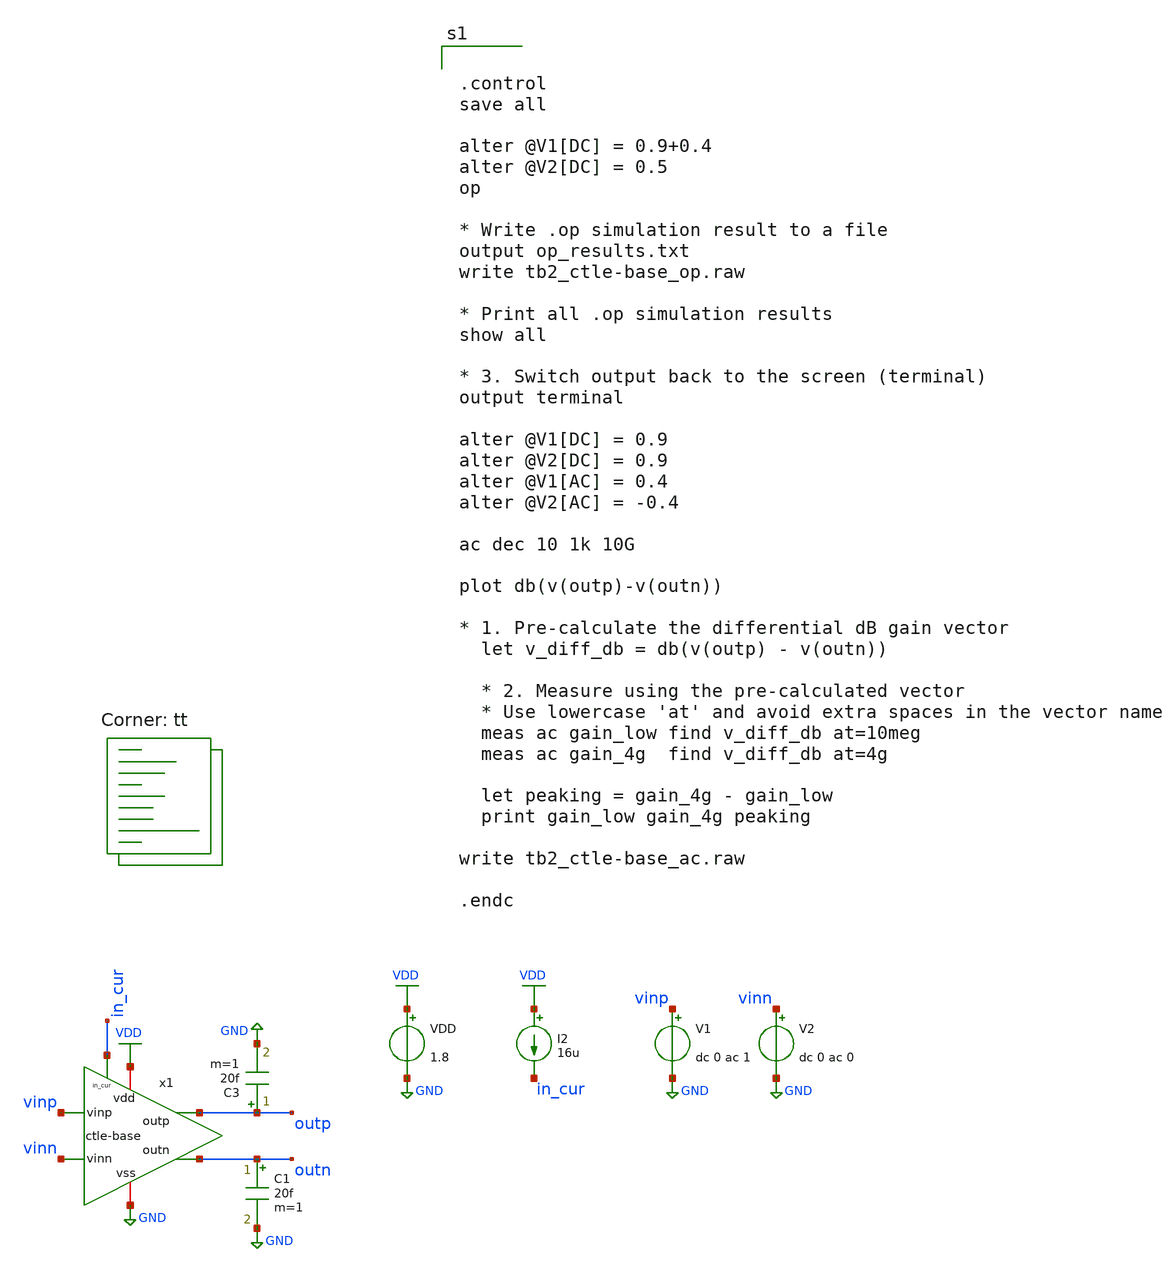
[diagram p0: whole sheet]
** sch_path: CTLE/tb2_ctle-base.sch
**.subckt tb2_ctle-base
x1 VDD GND outp outn vinn vinp in_cur ctle-base
VDD VDD GND 1.8
V1 vinp GND dc 0 ac 1
V2 vinn GND dc 0 ac 0
I2 VDD in_cur 16u
C3 outp GND 20f m=1
C1 outn GND 20f m=1
**** begin user architecture code
.lib $::SKYWATER_MODELS/sky130.lib.spice tt


.control
save all

alter @V1[DC] = 0.9+0.4
alter @V2[DC] = 0.5
op

* Write .op simulation result to a file
output op_results.txt
write tb2_ctle-base_op.raw

* Print all .op simulation results
show all

* 3. Switch output back to the screen (terminal)
output terminal

alter @V1[DC] = 0.9
alter @V2[DC] = 0.9
alter @V1[AC] = 0.4
alter @V2[AC] = -0.4

ac dec 10 1k 10G

plot db(v(outp)-v(outn))

* 1. Pre-calculate the differential dB gain vector
  let v_diff_db = db(v(outp) - v(outn))

  * 2. Measure using the pre-calculated vector
  * Use lowercase 'at' and avoid extra spaces in the vector name
  meas ac gain_low find v_diff_db at=10meg
  meas ac gain_4g  find v_diff_db at=4g

  let peaking = gain_4g - gain_low
  print gain_low gain_4g peaking

write tb2_ctle-base_ac.raw

.endc

**** end user architecture code
**.ends

* expanding   symbol:  /foss/designs/Teknofest/afe-icdec-teknofest-2026/CTLE/ctle-base.sym # of
*+ pins=7
** sym_path: CTLE/ctle-base.sym
** sch_path: CTLE/ctle-base.sch
.subckt ctle-base vdd vss outp outn vinn vinp in_cur
*.iopin vdd
*.iopin vss
*.ipin vinp
*.ipin vinn
*.opin outn
*.opin outp
*.ipin in_cur
XM1 outn vinp net1 net1 sky130_fd_pr__nfet_01v8 L=0.15 W=12.5 nf=1 ad='int((nf+1)/2) * W/nf * 0.29' as='int((nf+2)/2) * W/nf * 0.29'
+ pd='2*int((nf+1)/2) * (W/nf + 0.29)' ps='2*int((nf+2)/2) * (W/nf + 0.29)' nrd='0.29 / W' nrs='0.29 / W'
+ sa=0 sb=0 sd=0 mult=1 m=1
XM2 outp vinn net2 net2 sky130_fd_pr__nfet_01v8 L=0.15 W=12.5 nf=1 ad='int((nf+1)/2) * W/nf * 0.29' as='int((nf+2)/2) * W/nf * 0.29'
+ pd='2*int((nf+1)/2) * (W/nf + 0.29)' ps='2*int((nf+2)/2) * (W/nf + 0.29)' nrd='0.29 / W' nrs='0.29 / W'
+ sa=0 sb=0 sd=0 mult=1 m=1
XC1 net1 net2 sky130_fd_pr__cap_mim_m3_1 W=7.5 L=7.5 MF=1 m=1
XM5 in_cur in_cur vss vss sky130_fd_pr__nfet_01v8 L=0.5 W=1 nf=1 ad='int((nf+1)/2) * W/nf * 0.29' as='int((nf+2)/2) * W/nf * 0.29'
+ pd='2*int((nf+1)/2) * (W/nf + 0.29)' ps='2*int((nf+2)/2) * (W/nf + 0.29)' nrd='0.29 / W' nrs='0.29 / W'
+ sa=0 sb=0 sd=0 mult=1 m=1
XM6 net1 in_cur vss vss sky130_fd_pr__nfet_01v8 L=0.5 W=21.88 nf=1 ad='int((nf+1)/2) * W/nf * 0.29' as='int((nf+2)/2) * W/nf * 0.29'
+ pd='2*int((nf+1)/2) * (W/nf + 0.29)' ps='2*int((nf+2)/2) * (W/nf + 0.29)' nrd='0.29 / W' nrs='0.29 / W'
+ sa=0 sb=0 sd=0 mult=1 m=1
XM7 net2 in_cur vss vss sky130_fd_pr__nfet_01v8 L=0.5 W=21.88 nf=1 ad='int((nf+1)/2) * W/nf * 0.29' as='int((nf+2)/2) * W/nf * 0.29'
+ pd='2*int((nf+1)/2) * (W/nf + 0.29)' ps='2*int((nf+2)/2) * (W/nf + 0.29)' nrd='0.29 / W' nrs='0.29 / W'
+ sa=0 sb=0 sd=0 mult=1 m=1
XR3 net1 net2 vss sky130_fd_pr__res_xhigh_po_0p35 L=0.45 mult=1 m=1
XR1 vdd outn vss sky130_fd_pr__res_xhigh_po_0p35 L=0.45 mult=1 m=1
XR2 vdd outp vss sky130_fd_pr__res_xhigh_po_0p35 L=0.45 mult=1 m=1
.ends

.GLOBAL GND
.GLOBAL VDD
.end
